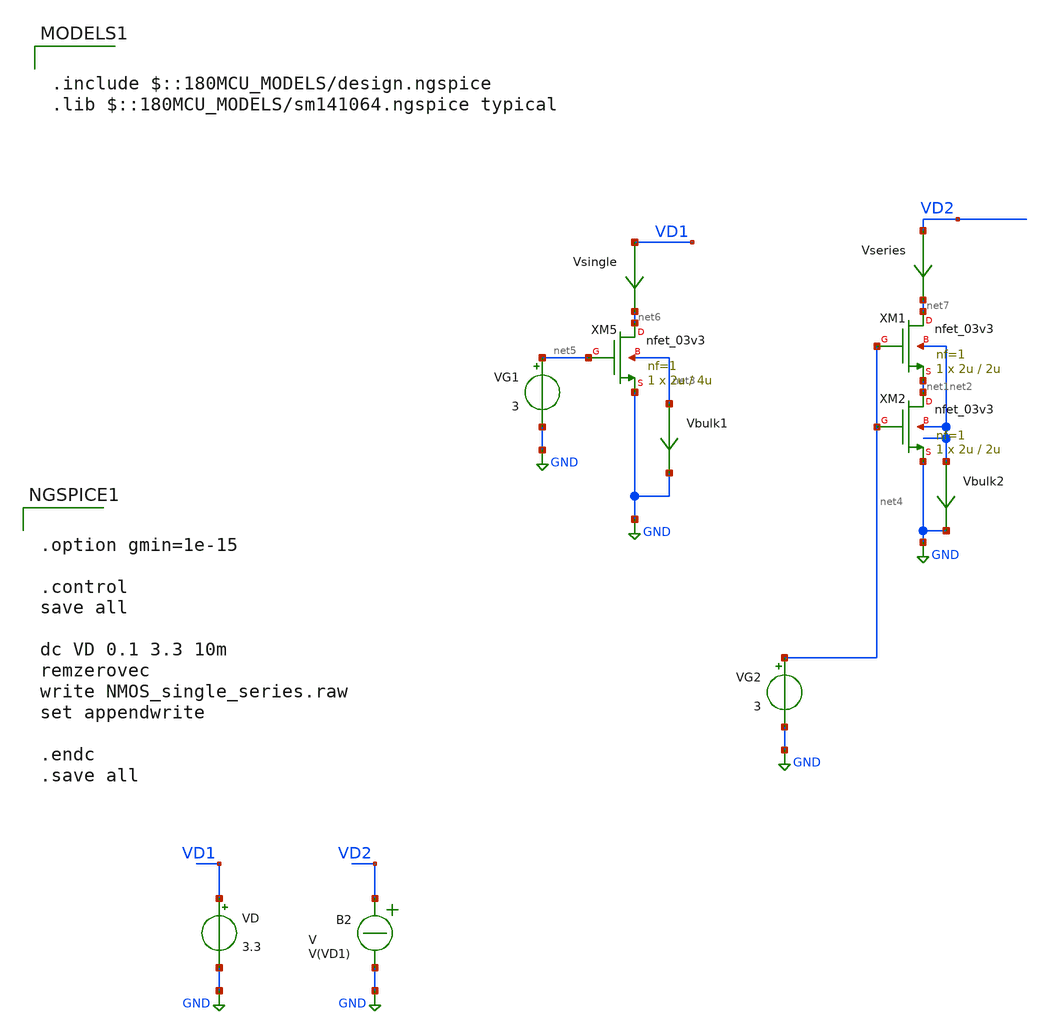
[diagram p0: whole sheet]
** sch_path: TIA_Filter/NMOS_single_series.sch
**.subckt NMOS_single_series
XM5 net6 net5 GND net3 nfet_03v3 L=4u W=2u nf=1 ad='int((nf+1)/2) * W/nf * 0.18u' as='int((nf+2)/2) * W/nf * 0.18u'
+ pd='2*int((nf+1)/2) * (W/nf + 0.18u)' ps='2*int((nf+2)/2) * (W/nf + 0.18u)' nrd='0.18u / W' nrs='0.18u / W'
+ sa=0 sb=0 sd=0 m=1
XM1 net7 net4 net1 net2 nfet_03v3 L=2u W=2u nf=1 ad='int((nf+1)/2) * W/nf * 0.18u' as='int((nf+2)/2) * W/nf * 0.18u'
+ pd='2*int((nf+1)/2) * (W/nf + 0.18u)' ps='2*int((nf+2)/2) * (W/nf + 0.18u)' nrd='0.18u / W' nrs='0.18u / W'
+ sa=0 sb=0 sd=0 m=1
XM2 net1 net4 GND net2 nfet_03v3 L=2u W=2u nf=1 ad='int((nf+1)/2) * W/nf * 0.18u' as='int((nf+2)/2) * W/nf * 0.18u'
+ pd='2*int((nf+1)/2) * (W/nf + 0.18u)' ps='2*int((nf+2)/2) * (W/nf + 0.18u)' nrd='0.18u / W' nrs='0.18u / W'
+ sa=0 sb=0 sd=0 m=1
VG2 net4 GND 3
VG1 net5 GND 3
Vsingle VD1 net6 0
.save i(vsingle)
VD VD1 GND 3.3
B2 VD2 GND V = V(VD1)
Vseries VD2 net7 0
.save i(vseries)
Vbulk1 net3 GND 0
.save i(vbulk1)
Vbulk2 net2 GND 0
.save i(vbulk2)
**** begin user architecture code


.option gmin=1e-15

.control
save all

dc VD 0.1 3.3 10m
remzerovec
write NMOS_single_series.raw
set appendwrite

.endc
.save all



.include $::180MCU_MODELS/design.ngspice
.lib $::180MCU_MODELS/sm141064.ngspice typical

**** end user architecture code
**.ends
.GLOBAL GND
.end
